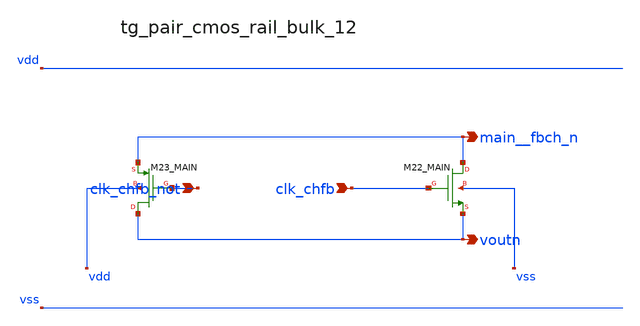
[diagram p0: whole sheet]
** sch_path: analog-db/raw/ia_004_fan_chopper_rrl/hier/blocks/tg_pair_cmos_rail_bulk_12.sch
**.subckt tg_pair_cmos_rail_bulk_12 clk_chfb_not clk_chfb main__fbch_n voutn
*.ipin clk_chfb_not
*.ipin clk_chfb
*.opin main__fbch_n
*.opin voutn
XM22_MAIN main__fbch_n clk_chfb voutn vss sg13_lv_nmos w=x_dut_xm22_main_w l=x_dut_xm22_main_l ng=1
+ m=x_dut_xm22_main_m
XM23_MAIN voutn clk_chfb_not main__fbch_n vdd sg13_lv_pmos w=x_dut_xm23_main_w l=x_dut_xm23_main_l
+ ng=1 m=x_dut_xm23_main_m
**.ends
.end
